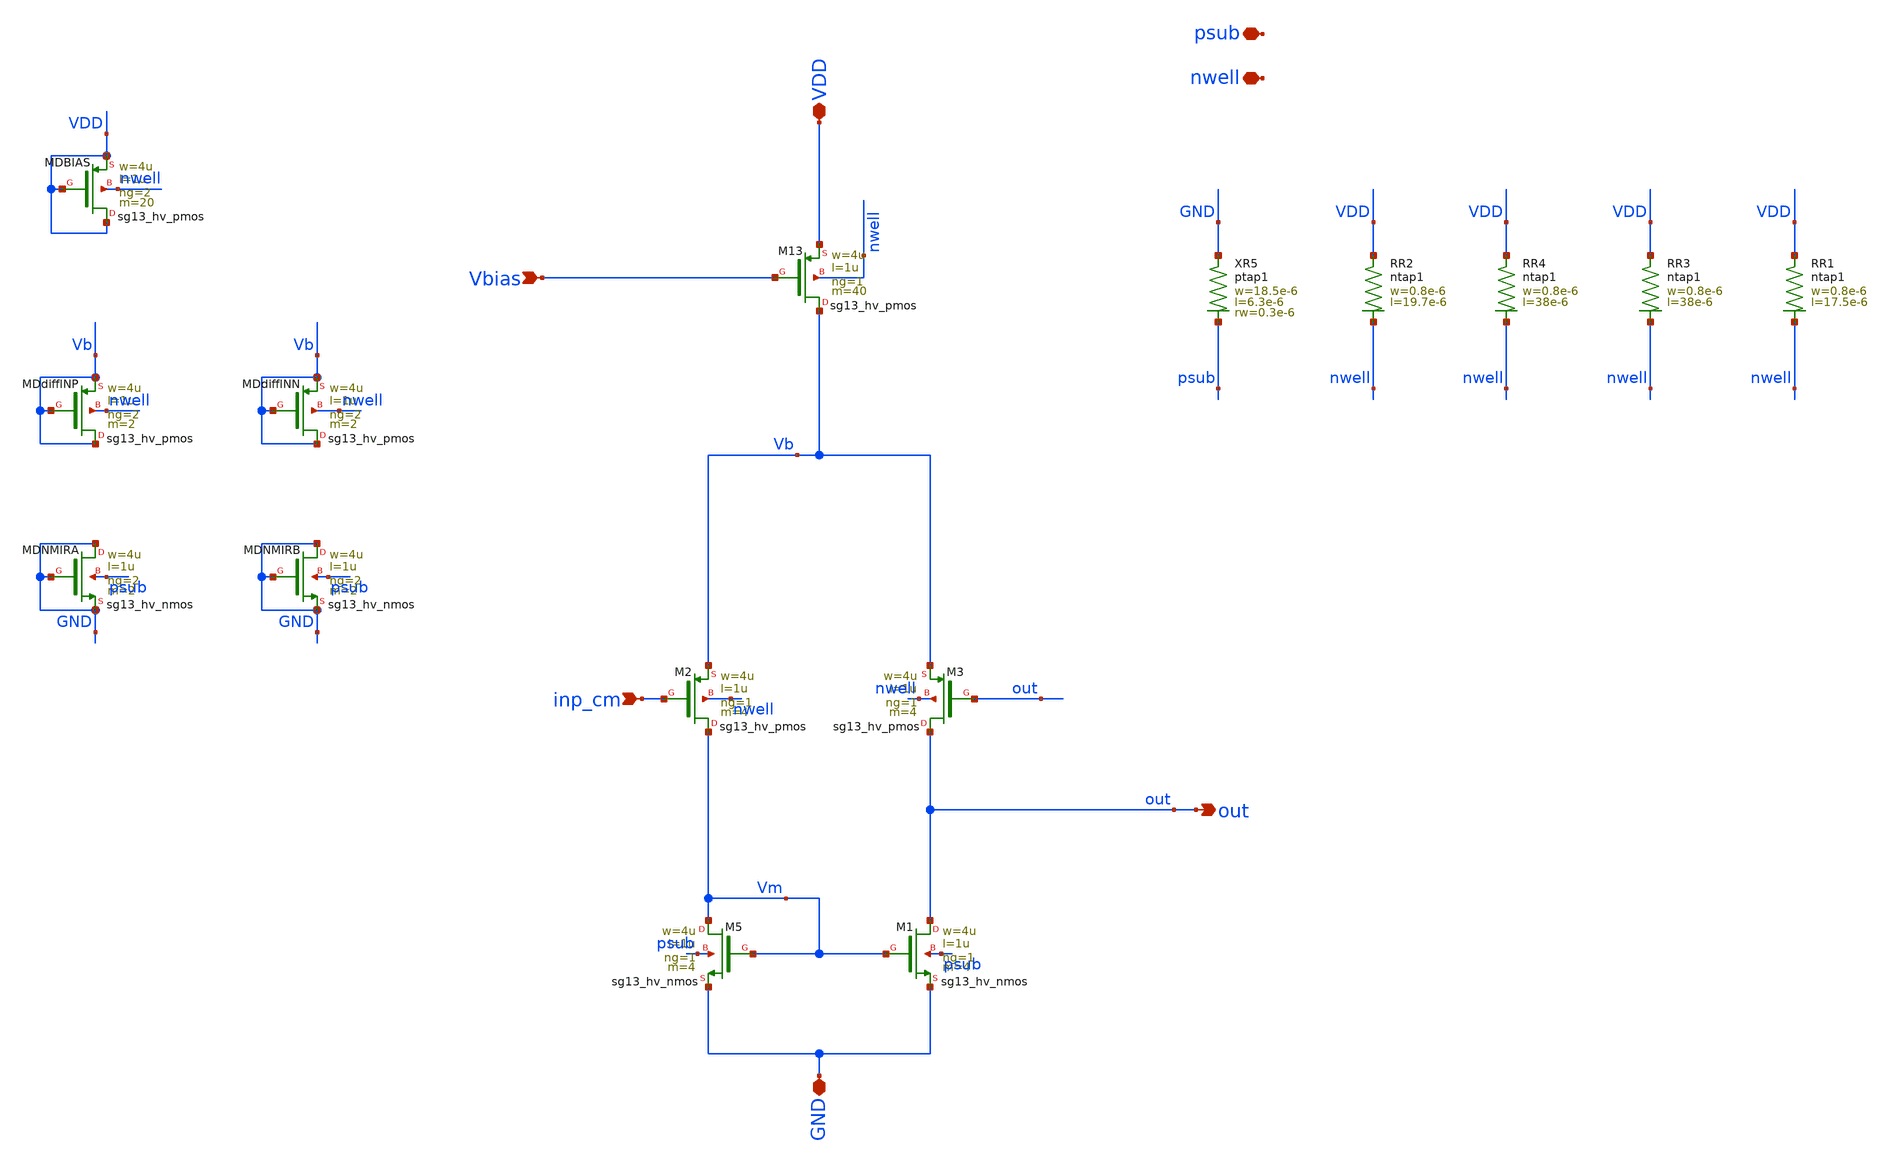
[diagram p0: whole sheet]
** sch_path: xschem/analog_buffer.sch
**.subckt analog_buffer inp_cm out VDD GND Vbias psub nwell
*.ipin inp_cm
*.opin out
*.iopin VDD
*.iopin GND
*.ipin Vbias
*.iopin psub
*.iopin nwell
XM2 Vm inp_cm Vb nwell sg13_hv_pmos w=4u l=1u ng=1 m=4 mm_ok=1
XM5 Vm Vm GND psub sg13_hv_nmos w=4u l=1u ng=1 m=4 mm_ok=1
XM13 Vb Vbias VDD nwell sg13_hv_pmos w=4u l=1u ng=1 m=40 mm_ok=1
XM3 out out Vb nwell sg13_hv_pmos w=4u l=1u ng=1 m=4 mm_ok=1
XM1 out Vm GND psub sg13_hv_nmos w=4u l=1u ng=1 m=4 mm_ok=1
XR2 VDD nwell ntap1 R=17.27 w=0.8e-6 l=19.7e-6
XMDBIAS VDD VDD VDD nwell sg13_hv_pmos w=4u l=1u ng=2 m=20 mm_ok=1
XMDdiffINP Vb Vb Vb nwell sg13_hv_pmos w=4u l=1u ng=2 m=2 mm_ok=1
XMDdiffINN Vb Vb Vb nwell sg13_hv_pmos w=4u l=1u ng=2 m=2 mm_ok=1
XMDNMIRA GND GND GND psub sg13_hv_nmos w=4u l=1u ng=2 m=2 mm_ok=1
XMDNMIRB GND GND GND psub sg13_hv_nmos w=4u l=1u ng=2 m=2 mm_ok=1
XR3 VDD nwell ntap1 R=9.074 w=0.8e-6 l=38e-6
XR4 VDD nwell ntap1 R=9.074 w=0.8e-6 l=38e-6
XR5 GND psub ptap1 R=4.709 w=18.5e-6 l=6.3e-6 rw=0.3e-6
XR1 VDD nwell ntap1 R=19.37 w=0.8e-6 l=17.5e-6
**.ends
.end
